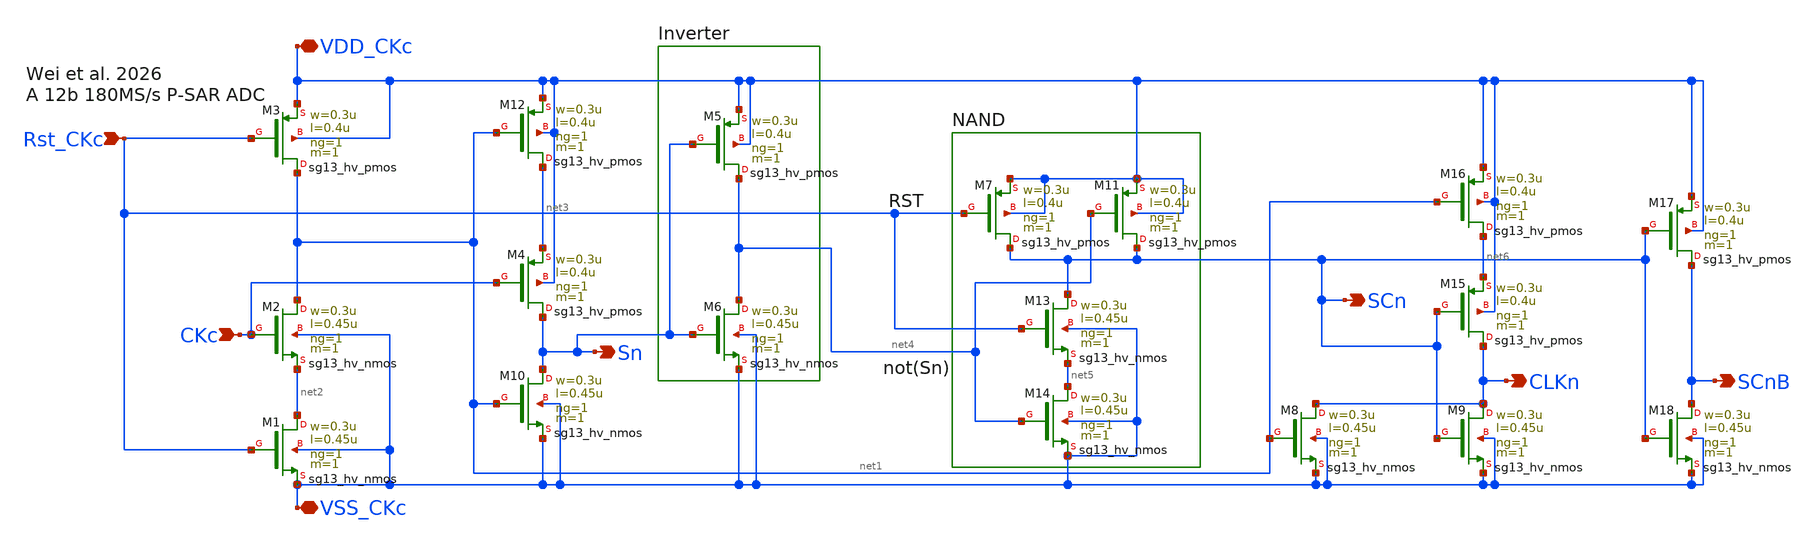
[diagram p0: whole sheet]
** sch_path: circuit_files/sar_adc_20260903/sarBitClk.sch
**.subckt sarBitClk CKc Rst_CKc VDD_CKc VSS_CKc Sn SCn CLKn SCnB
*.ipin CKc
*.ipin Rst_CKc
*.iopin VDD_CKc
*.iopin VSS_CKc
*.opin Sn
*.opin SCn
*.opin CLKn
*.opin SCnB
XM1 net2 Rst_CKc VSS_CKc VSS_CKc sg13_hv_nmos w=0.3u l=0.45u ng=1 m=1 mm_ok=1
XM3 net1 Rst_CKc VDD_CKc VDD_CKc sg13_hv_pmos w=0.3u l=0.4u ng=1 m=1 mm_ok=1
XM12 net3 net1 VDD_CKc VDD_CKc sg13_hv_pmos w=0.3u l=0.4u ng=1 m=1 mm_ok=1
XM10 Sn net1 VSS_CKc VSS_CKc sg13_hv_nmos w=0.3u l=0.45u ng=1 m=1 mm_ok=1
XM2 net1 CKc net2 VSS_CKc sg13_hv_nmos w=0.3u l=0.45u ng=1 m=1 mm_ok=1
XM4 Sn CKc net3 VDD_CKc sg13_hv_pmos w=0.3u l=0.4u ng=1 m=1 mm_ok=1
XM5 net4 Sn VDD_CKc VDD_CKc sg13_hv_pmos w=0.3u l=0.4u ng=1 m=1 mm_ok=1
XM6 net4 Sn VSS_CKc VSS_CKc sg13_hv_nmos w=0.3u l=0.45u ng=1 m=1 mm_ok=1
XM11 SCn net4 VDD_CKc VDD_CKc sg13_hv_pmos w=0.3u l=0.4u ng=1 m=1 mm_ok=1
XM7 SCn Rst_CKc VDD_CKc VDD_CKc sg13_hv_pmos w=0.3u l=0.4u ng=1 m=1 mm_ok=1
XM13 SCn Rst_CKc net5 VSS_CKc sg13_hv_nmos w=0.3u l=0.45u ng=1 m=1 mm_ok=1
XM14 net5 net4 VSS_CKc VSS_CKc sg13_hv_nmos w=0.3u l=0.45u ng=1 m=1 mm_ok=1
XM8 CLKn net1 VSS_CKc VSS_CKc sg13_hv_nmos w=0.3u l=0.45u ng=1 m=1 mm_ok=1
XM9 CLKn SCn VSS_CKc VSS_CKc sg13_hv_nmos w=0.3u l=0.45u ng=1 m=1 mm_ok=1
XM15 CLKn SCn net6 VDD_CKc sg13_hv_pmos w=0.3u l=0.4u ng=1 m=1 mm_ok=1
XM16 net6 net1 VDD_CKc VDD_CKc sg13_hv_pmos w=0.3u l=0.4u ng=1 m=1 mm_ok=1
XM17 SCnB SCn VDD_CKc VDD_CKc sg13_hv_pmos w=0.3u l=0.4u ng=1 m=1 mm_ok=1
XM18 SCnB SCn VSS_CKc VSS_CKc sg13_hv_nmos w=0.3u l=0.45u ng=1 m=1 mm_ok=1
**.ends
.end
